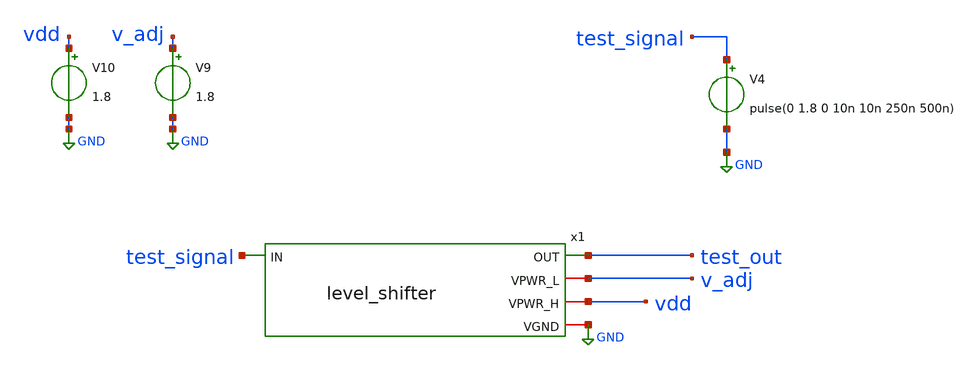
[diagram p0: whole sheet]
** sch_path: xschem/tb_level.sch
**.subckt tb_level
V4 test_signal GND pulse(0 1.8 0 10n 10n 250n 500n)
V9 v_adj GND 1.8
V10 vdd GND 1.8
x1 test_out v_adj test_signal vdd GND level_shifter
**** begin user architecture code

** opencircuitdesign pdks install
.lib $::SKYWATER_MODELS/sky130.lib.spice tt




* .options filetype=ascii
.control
  let vstart = 1.8
  let vstop = 0.5
  let vstep = -0.1
  let vcurrent = vstart
  while vcurrent >= vstop
    alter V9 vcurrent
    alter @V4[PULSE] [ 0 {vcurrent} 0 10n 10n 200n 500n ]
    tran 0.1n 1u
    write tb_level.raw
    set appendwrite

    let vcurrent = vcurrent + vstep
  end
.endc

.end


**** end user architecture code
**.ends

* expanding   symbol:  level_shifter.sym # of pins=5
** sym_path: xschem/level_shifter.sym
** sch_path: xschem/level_shifter.sch
.subckt level_shifter OUT VPWR_L IN VPWR_H VGND
*.iopin VGND
*.iopin VPWR_H
*.iopin VPWR_L
*.ipin IN
*.opin OUT
XM1 net2 OUT VPWR_H VPWR_H sky130_fd_pr__pfet_01v8 L=0.15 W=2 nf=1 ad='int((nf+1)/2) * W/nf * 0.29' as='int((nf+2)/2) * W/nf * 0.29'
+ pd='2*int((nf+1)/2) * (W/nf + 0.29)' ps='2*int((nf+2)/2) * (W/nf + 0.29)' nrd='0.29 / W' nrs='0.29 / W'
+ sa=0 sb=0 sd=0 mult=1 m=1
XM2 OUT net2 VPWR_H VPWR_H sky130_fd_pr__pfet_01v8 L=0.15 W=2 nf=1 ad='int((nf+1)/2) * W/nf * 0.29' as='int((nf+2)/2) * W/nf * 0.29'
+ pd='2*int((nf+1)/2) * (W/nf + 0.29)' ps='2*int((nf+2)/2) * (W/nf + 0.29)' nrd='0.29 / W' nrs='0.29 / W'
+ sa=0 sb=0 sd=0 mult=1 m=1
XM3 net2 IN VGND VGND sky130_fd_pr__nfet_01v8 L=0.15 W=1 nf=1 ad='int((nf+1)/2) * W/nf * 0.29' as='int((nf+2)/2) * W/nf * 0.29'
+ pd='2*int((nf+1)/2) * (W/nf + 0.29)' ps='2*int((nf+2)/2) * (W/nf + 0.29)' nrd='0.29 / W' nrs='0.29 / W'
+ sa=0 sb=0 sd=0 mult=1 m=1
XM4 OUT net1 VGND VGND sky130_fd_pr__nfet_01v8 L=0.15 W=1 nf=1 ad='int((nf+1)/2) * W/nf * 0.29' as='int((nf+2)/2) * W/nf * 0.29'
+ pd='2*int((nf+1)/2) * (W/nf + 0.29)' ps='2*int((nf+2)/2) * (W/nf + 0.29)' nrd='0.29 / W' nrs='0.29 / W'
+ sa=0 sb=0 sd=0 mult=1 m=1
XM5 net1 IN VPWR_L VPWR_L sky130_fd_pr__pfet_01v8 L=0.15 W=2 nf=1 ad='int((nf+1)/2) * W/nf * 0.29' as='int((nf+2)/2) * W/nf * 0.29'
+ pd='2*int((nf+1)/2) * (W/nf + 0.29)' ps='2*int((nf+2)/2) * (W/nf + 0.29)' nrd='0.29 / W' nrs='0.29 / W'
+ sa=0 sb=0 sd=0 mult=1 m=1
XM6 net1 IN VGND VGND sky130_fd_pr__nfet_01v8 L=0.15 W=1 nf=1 ad='int((nf+1)/2) * W/nf * 0.29' as='int((nf+2)/2) * W/nf * 0.29'
+ pd='2*int((nf+1)/2) * (W/nf + 0.29)' ps='2*int((nf+2)/2) * (W/nf + 0.29)' nrd='0.29 / W' nrs='0.29 / W'
+ sa=0 sb=0 sd=0 mult=1 m=1
.ends

.GLOBAL GND
.end
